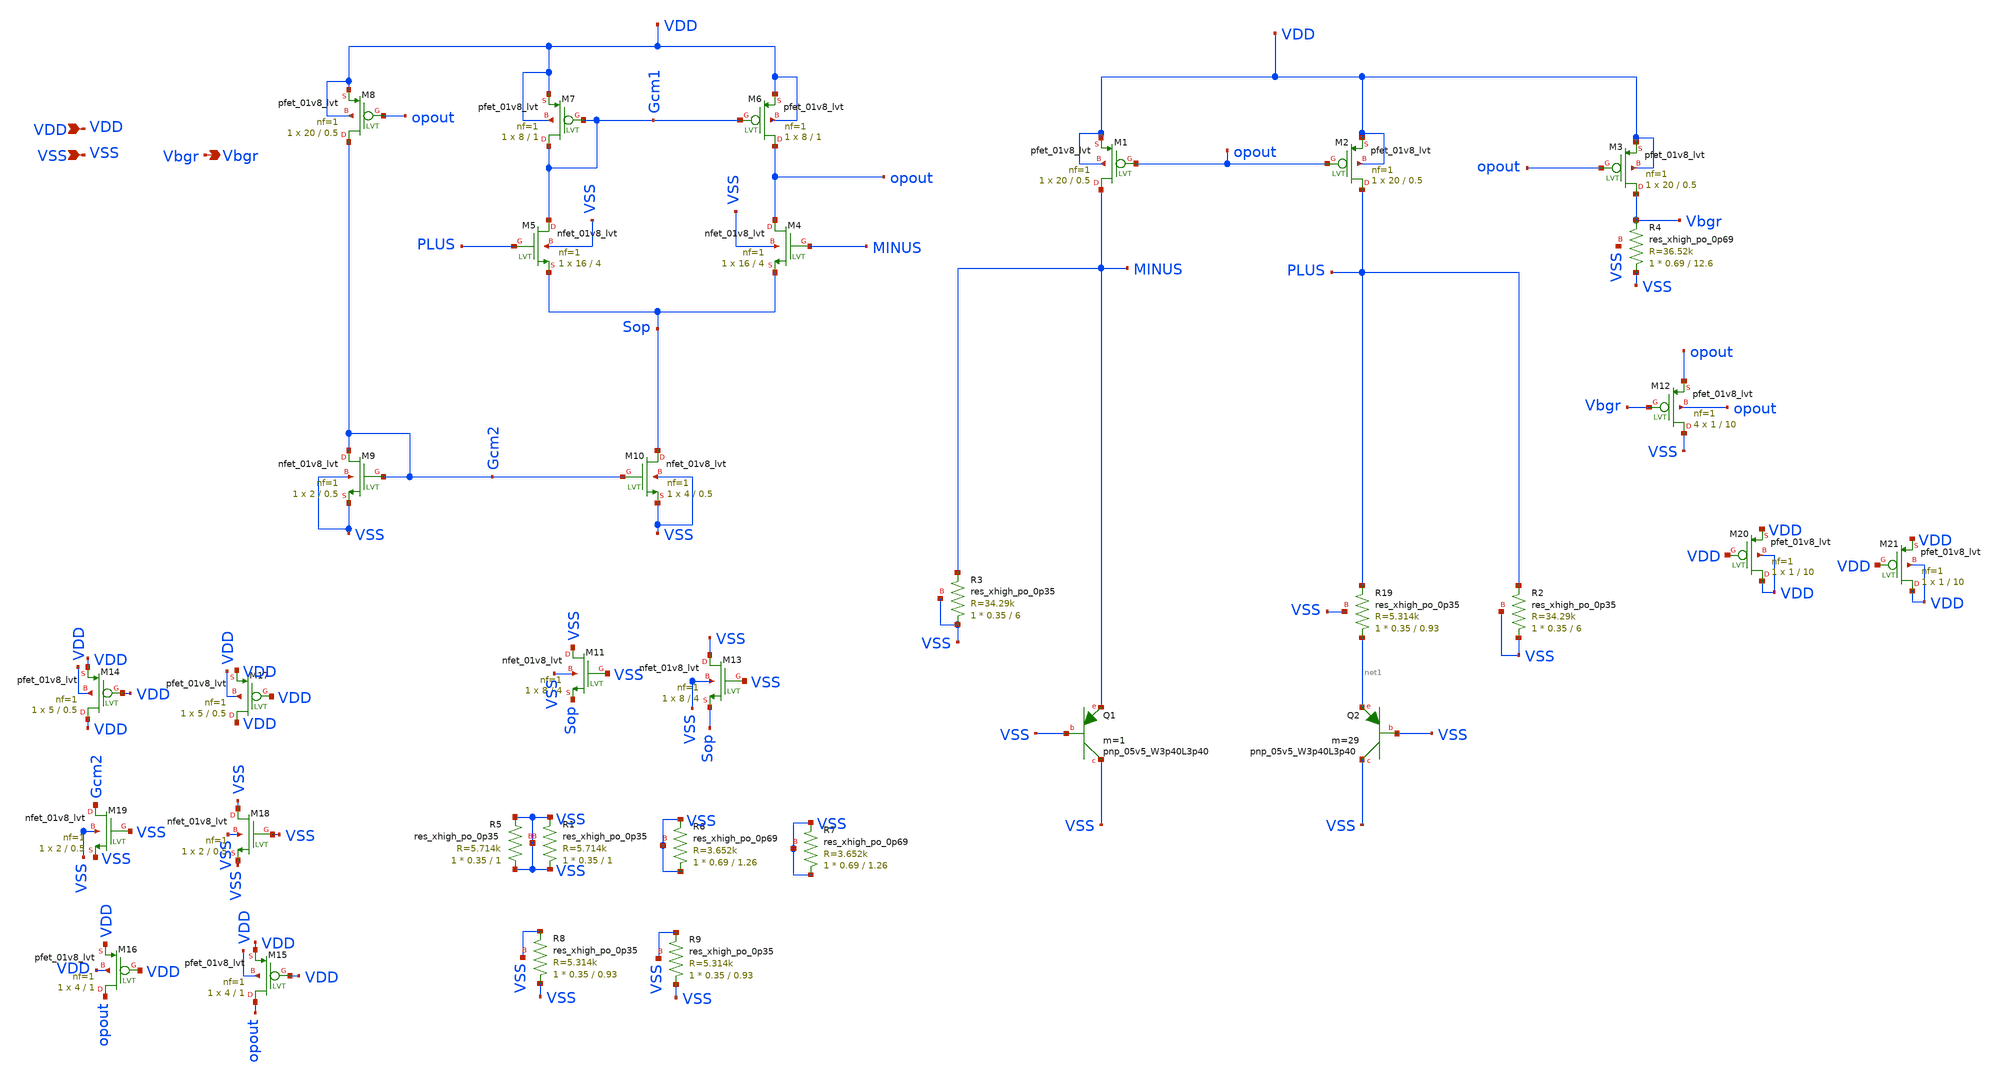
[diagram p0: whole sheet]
** sch_path: custom_gds/tt_um_bgr_agolmanesh/xschem/core_prel.sch
**.subckt core_prel VDD VSS Vbgr
*.ipin VDD
*.ipin VSS
*.opin Vbgr
XQ1 VSS VSS MINUS sky130_fd_pr__pnp_05v5_W3p40L3p40 m=1
XQ2 VSS VSS net1 sky130_fd_pr__pnp_05v5_W3p40L3p40 m=29
XM1 MINUS opout VDD VDD sky130_fd_pr__pfet_01v8_lvt L=0.5 W=20 nf=1 ad='int((nf+1)/2) * W/nf * 0.29'
+ as='int((nf+2)/2) * W/nf * 0.29' pd='2*int((nf+1)/2) * (W/nf + 0.29)' ps='2*int((nf+2)/2) * (W/nf + 0.29)'
+ nrd='0.29 / W' nrs='0.29 / W' sa=0 sb=0 sd=0 mult=1 m=1
XM2 PLUS opout VDD VDD sky130_fd_pr__pfet_01v8_lvt L=0.5 W=20 nf=1 ad='int((nf+1)/2) * W/nf * 0.29' as='int((nf+2)/2) * W/nf * 0.29'
+ pd='2*int((nf+1)/2) * (W/nf + 0.29)' ps='2*int((nf+2)/2) * (W/nf + 0.29)' nrd='0.29 / W' nrs='0.29 / W'
+ sa=0 sb=0 sd=0 mult=1 m=1
XM3 Vbgr opout VDD VDD sky130_fd_pr__pfet_01v8_lvt L=0.5 W=20 nf=1 ad='int((nf+1)/2) * W/nf * 0.29' as='int((nf+2)/2) * W/nf * 0.29'
+ pd='2*int((nf+1)/2) * (W/nf + 0.29)' ps='2*int((nf+2)/2) * (W/nf + 0.29)' nrd='0.29 / W' nrs='0.29 / W'
+ sa=0 sb=0 sd=0 mult=1 m=1
XM4 opout MINUS Sop VSS sky130_fd_pr__nfet_01v8_lvt L=4 W=16 nf=1 ad='int((nf+1)/2) * W/nf * 0.29' as='int((nf+2)/2) * W/nf * 0.29'
+ pd='2*int((nf+1)/2) * (W/nf + 0.29)' ps='2*int((nf+2)/2) * (W/nf + 0.29)' nrd='0.29 / W' nrs='0.29 / W'
+ sa=0 sb=0 sd=0 mult=1 m=1
XM5 Gcm1 PLUS Sop VSS sky130_fd_pr__nfet_01v8_lvt L=4 W=16 nf=1 ad='int((nf+1)/2) * W/nf * 0.29' as='int((nf+2)/2) * W/nf * 0.29'
+ pd='2*int((nf+1)/2) * (W/nf + 0.29)' ps='2*int((nf+2)/2) * (W/nf + 0.29)' nrd='0.29 / W' nrs='0.29 / W'
+ sa=0 sb=0 sd=0 mult=1 m=1
XM6 opout Gcm1 VDD VDD sky130_fd_pr__pfet_01v8_lvt L=1 W=8 nf=1 ad='int((nf+1)/2) * W/nf * 0.29' as='int((nf+2)/2) * W/nf * 0.29'
+ pd='2*int((nf+1)/2) * (W/nf + 0.29)' ps='2*int((nf+2)/2) * (W/nf + 0.29)' nrd='0.29 / W' nrs='0.29 / W'
+ sa=0 sb=0 sd=0 mult=1 m=1
XM10 Sop Gcm2 VSS VSS sky130_fd_pr__nfet_01v8_lvt L=0.5 W=4 nf=1 ad='int((nf+1)/2) * W/nf * 0.29' as='int((nf+2)/2) * W/nf * 0.29'
+ pd='2*int((nf+1)/2) * (W/nf + 0.29)' ps='2*int((nf+2)/2) * (W/nf + 0.29)' nrd='0.29 / W' nrs='0.29 / W'
+ sa=0 sb=0 sd=0 mult=1 m=1
XM9 Gcm2 Gcm2 VSS VSS sky130_fd_pr__nfet_01v8_lvt L=0.5 W=2 nf=1 ad='int((nf+1)/2) * W/nf * 0.29' as='int((nf+2)/2) * W/nf * 0.29'
+ pd='2*int((nf+1)/2) * (W/nf + 0.29)' ps='2*int((nf+2)/2) * (W/nf + 0.29)' nrd='0.29 / W' nrs='0.29 / W'
+ sa=0 sb=0 sd=0 mult=1 m=1
XM7 Gcm1 Gcm1 VDD VDD sky130_fd_pr__pfet_01v8_lvt L=1 W=8 nf=1 ad='int((nf+1)/2) * W/nf * 0.29' as='int((nf+2)/2) * W/nf * 0.29'
+ pd='2*int((nf+1)/2) * (W/nf + 0.29)' ps='2*int((nf+2)/2) * (W/nf + 0.29)' nrd='0.29 / W' nrs='0.29 / W'
+ sa=0 sb=0 sd=0 mult=1 m=1
XM8 Gcm2 opout VDD VDD sky130_fd_pr__pfet_01v8_lvt L=0.5 W=20 nf=1 ad='int((nf+1)/2) * W/nf * 0.29' as='int((nf+2)/2) * W/nf * 0.29'
+ pd='2*int((nf+1)/2) * (W/nf + 0.29)' ps='2*int((nf+2)/2) * (W/nf + 0.29)' nrd='0.29 / W' nrs='0.29 / W'
+ sa=0 sb=0 sd=0 mult=1 m=1
XR19 net1 PLUS VSS sky130_fd_pr__res_xhigh_po_0p35 L=0.93 mult=1 m=1
XR3 VSS MINUS VSS sky130_fd_pr__res_xhigh_po_0p35 L=6 mult=1 m=1
XR4 VSS Vbgr VSS sky130_fd_pr__res_xhigh_po_0p69 L=12.6 mult=1 m=1
XM12 VSS Vbgr opout opout sky130_fd_pr__pfet_01v8_lvt L=10 W=1 nf=1 ad='int((nf+1)/2) * W/nf * 0.29'
+ as='int((nf+2)/2) * W/nf * 0.29' pd='2*int((nf+1)/2) * (W/nf + 0.29)' ps='2*int((nf+2)/2) * (W/nf + 0.29)'
+ nrd='0.29 / W' nrs='0.29 / W' sa=0 sb=0 sd=0 mult=4 m=4
XR2 VSS PLUS VSS sky130_fd_pr__res_xhigh_po_0p35 L=6 mult=1 m=1
XR1 VSS VSS VSS sky130_fd_pr__res_xhigh_po_0p35 L=1 mult=1 m=1
XR5 VSS VSS VSS sky130_fd_pr__res_xhigh_po_0p35 L=1 mult=1 m=1
XR6 VSS VSS VSS sky130_fd_pr__res_xhigh_po_0p69 L=1.26 mult=1 m=1
XM17 VDD VDD VDD VDD sky130_fd_pr__pfet_01v8_lvt L=0.5 W=5 nf=1 ad='int((nf+1)/2) * W/nf * 0.29' as='int((nf+2)/2) * W/nf * 0.29'
+ pd='2*int((nf+1)/2) * (W/nf + 0.29)' ps='2*int((nf+2)/2) * (W/nf + 0.29)' nrd='0.29 / W' nrs='0.29 / W'
+ sa=0 sb=0 sd=0 mult=1 m=1
XM18 VSS VSS VSS VSS sky130_fd_pr__nfet_01v8_lvt L=0.5 W=2 nf=1 ad='int((nf+1)/2) * W/nf * 0.29' as='int((nf+2)/2) * W/nf * 0.29'
+ pd='2*int((nf+1)/2) * (W/nf + 0.29)' ps='2*int((nf+2)/2) * (W/nf + 0.29)' nrd='0.29 / W' nrs='0.29 / W'
+ sa=0 sb=0 sd=0 mult=1 m=1
XM19 Gcm2 VSS VSS VSS sky130_fd_pr__nfet_01v8_lvt L=0.5 W=2 nf=1 ad='int((nf+1)/2) * W/nf * 0.29' as='int((nf+2)/2) * W/nf * 0.29'
+ pd='2*int((nf+1)/2) * (W/nf + 0.29)' ps='2*int((nf+2)/2) * (W/nf + 0.29)' nrd='0.29 / W' nrs='0.29 / W'
+ sa=0 sb=0 sd=0 mult=1 m=1
XR7 VSS VSS VSS sky130_fd_pr__res_xhigh_po_0p69 L=1.26 mult=1 m=1
XM20 VDD VDD VDD VDD sky130_fd_pr__pfet_01v8_lvt L=10 W=1 nf=1 ad='int((nf+1)/2) * W/nf * 0.29' as='int((nf+2)/2) * W/nf * 0.29'
+ pd='2*int((nf+1)/2) * (W/nf + 0.29)' ps='2*int((nf+2)/2) * (W/nf + 0.29)' nrd='0.29 / W' nrs='0.29 / W'
+ sa=0 sb=0 sd=0 mult=1 m=1
XR8 VSS VSS VSS sky130_fd_pr__res_xhigh_po_0p35 L=0.93 mult=1 m=1
XR9 VSS VSS VSS sky130_fd_pr__res_xhigh_po_0p35 L=0.93 mult=1 m=1
XM21 VDD VDD VDD VDD sky130_fd_pr__pfet_01v8_lvt L=10 W=1 nf=1 ad='int((nf+1)/2) * W/nf * 0.29' as='int((nf+2)/2) * W/nf * 0.29'
+ pd='2*int((nf+1)/2) * (W/nf + 0.29)' ps='2*int((nf+2)/2) * (W/nf + 0.29)' nrd='0.29 / W' nrs='0.29 / W'
+ sa=0 sb=0 sd=0 mult=1 m=1
XM11 VSS VSS Sop VSS sky130_fd_pr__nfet_01v8_lvt L=4 W=8 nf=1 ad='int((nf+1)/2) * W/nf * 0.29' as='int((nf+2)/2) * W/nf * 0.29'
+ pd='2*int((nf+1)/2) * (W/nf + 0.29)' ps='2*int((nf+2)/2) * (W/nf + 0.29)' nrd='0.29 / W' nrs='0.29 / W'
+ sa=0 sb=0 sd=0 mult=1 m=1
XM13 VSS VSS Sop VSS sky130_fd_pr__nfet_01v8_lvt L=4 W=8 nf=1 ad='int((nf+1)/2) * W/nf * 0.29' as='int((nf+2)/2) * W/nf * 0.29'
+ pd='2*int((nf+1)/2) * (W/nf + 0.29)' ps='2*int((nf+2)/2) * (W/nf + 0.29)' nrd='0.29 / W' nrs='0.29 / W'
+ sa=0 sb=0 sd=0 mult=1 m=1
XM14 VDD VDD VDD VDD sky130_fd_pr__pfet_01v8_lvt L=0.5 W=5 nf=1 ad='int((nf+1)/2) * W/nf * 0.29' as='int((nf+2)/2) * W/nf * 0.29'
+ pd='2*int((nf+1)/2) * (W/nf + 0.29)' ps='2*int((nf+2)/2) * (W/nf + 0.29)' nrd='0.29 / W' nrs='0.29 / W'
+ sa=0 sb=0 sd=0 mult=1 m=1
XM15 opout VDD VDD VDD sky130_fd_pr__pfet_01v8_lvt L=1 W=4 nf=1 ad='int((nf+1)/2) * W/nf * 0.29' as='int((nf+2)/2) * W/nf * 0.29'
+ pd='2*int((nf+1)/2) * (W/nf + 0.29)' ps='2*int((nf+2)/2) * (W/nf + 0.29)' nrd='0.29 / W' nrs='0.29 / W'
+ sa=0 sb=0 sd=0 mult=1 m=1
XM16 opout VDD VDD VDD sky130_fd_pr__pfet_01v8_lvt L=1 W=4 nf=1 ad='int((nf+1)/2) * W/nf * 0.29' as='int((nf+2)/2) * W/nf * 0.29'
+ pd='2*int((nf+1)/2) * (W/nf + 0.29)' ps='2*int((nf+2)/2) * (W/nf + 0.29)' nrd='0.29 / W' nrs='0.29 / W'
+ sa=0 sb=0 sd=0 mult=1 m=1
**** begin user architecture code

** opencircuitdesign pdks install
.lib $::SKYWATER_MODELS/sky130.lib.spice tt


**** end user architecture code
**.ends
.end
